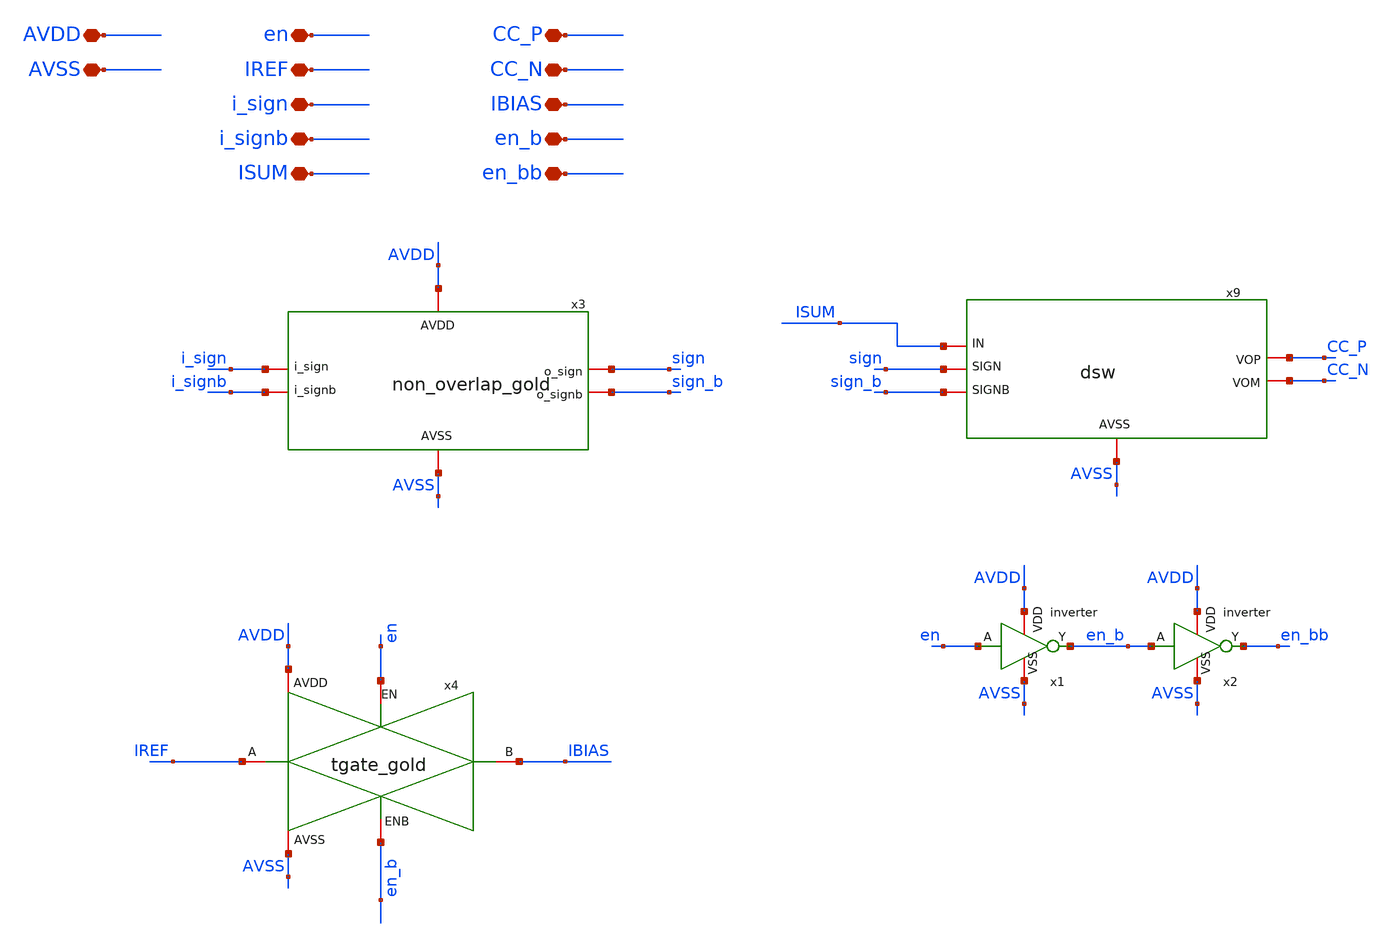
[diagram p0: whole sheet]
** sch_path: current_generator/analog/DAC/schematics/sub_top_gold.sch
**.subckt sub_top_gold AVDD AVSS en en_b en_bb i_sign i_signb ISUM CC_P CC_N IREF IBIAS
*.iopin AVDD
*.iopin AVSS
*.iopin en
*.iopin en_b
*.iopin en_bb
*.iopin i_sign
*.iopin i_signb
*.iopin ISUM
*.iopin CC_P
*.iopin CC_N
*.iopin IREF
*.iopin IBIAS
x9 sign sign_b ISUM AVSS CC_P CC_N dsw
x1 en en_b AVDD AVSS inverter
x2 en_b en_bb AVDD AVSS inverter
x3 AVDD AVSS i_signb i_sign sign sign_b non_overlap_gold
x4 AVDD AVSS en en_b IREF IBIAS tgate_gold
**.ends

* expanding   symbol:  dsw.sym # of pins=6
** sym_path: current_generator/analog/DAC/dsw.sym
** sch_path: current_generator/analog/DAC/dsw.sch
.subckt dsw SIGN SIGNB IN AVSS VOP VOM
*.iopin SIGN
*.iopin SIGNB
*.iopin IN
*.iopin AVSS
*.iopin VOP
*.iopin VOM
XM1 IN SIGN VOM AVSS sg13_lv_nmos w=3u l=0.13u ng=1 m=2 mm_ok=1
XM2 VOM SIGNB AVSS AVSS sg13_lv_nmos w=3u l=0.13u ng=1 m=2 mm_ok=1
XM3 IN SIGNB VOP AVSS sg13_lv_nmos w=3u l=0.13u ng=1 m=2 mm_ok=1
XM4 VOP SIGN AVSS AVSS sg13_lv_nmos w=3u l=0.13u ng=1 m=2 mm_ok=1
.ends


* expanding   symbol:  inverter.sym # of pins=4
** sym_path: current_generator/analog/DAC/schematics/inverter.sym
** sch_path: current_generator/analog/DAC/schematics/inverter.sch
.subckt inverter A Y VDD VSS
*.opin Y
*.ipin A
*.iopin VDD
*.iopin VSS
MMN0 Y A VSS VSS sg13_lv_nmos w=740.00n l=130.00n ng=1 m=1 mm_ok=1
MMP0 Y A VDD VDD sg13_lv_pmos w=1.12u l=130.00n ng=1 m=1 mm_ok=1
.ends


* expanding   symbol:  non_overlap_gold.sym # of pins=6
** sym_path: current_generator/analog/DAC/schematics/non_overlap_gold.sym
** sch_path: current_generator/analog/DAC/schematics/non_overlap_gold.sch
.subckt non_overlap_gold AVDD AVSS i_signb i_sign o_sign o_signb
*.iopin AVDD
*.iopin AVSS
*.iopin i_sign
*.iopin i_signb
*.iopin o_sign
*.iopin o_signb
x5 AVDD AVSS i_sign xb xa nand
x6 xa o_sign AVDD AVSS inverter
x3 AVDD AVSS i_signb xa xb nand
x1 xb o_signb AVDD AVSS inverter
.ends


* expanding   symbol:  tgate_gold.sym # of pins=6
** sym_path: current_generator/analog/DAC/schematics/tgate_gold.sym
** sch_path: current_generator/analog/DAC/schematics/tgate_gold.sch
.subckt tgate_gold AVDD AVSS EN ENB A B
*.iopin AVDD
*.iopin AVSS
*.iopin EN
*.iopin ENB
*.iopin A
*.iopin B
XM1 A EN B AVSS sg13_lv_nmos w=1u l=1u ng=1 m=2 mm_ok=1
XM2 B ENB A AVDD sg13_lv_pmos w=1u l=1u ng=1 m=2 mm_ok=1
.ends


* expanding   symbol:  nand.sym # of pins=5
** sym_path: current_generator/analog/DAC/schematics/nand.sym
** sch_path: current_generator/analog/DAC/schematics/nand.sch
.subckt nand VDD VSS A B Y
*.opin Y
*.ipin A
*.iopin VDD
*.iopin VSS
*.ipin B
XMN0 net1 B VSS VSS sg13_lv_nmos w=1.44u l=130.00n ng=2 m=1 mm_ok=1
XMP0 Y B VDD VDD sg13_lv_pmos w=2.24u l=130.00n ng=2 m=1 mm_ok=1
XMN1 Y A net1 VSS sg13_lv_nmos w=1.44u l=130.00n ng=2 m=1 mm_ok=1
XMP1 Y A VDD VDD sg13_lv_pmos w=2.24u l=130.00n ng=2 m=1 mm_ok=1
.ends

.end
